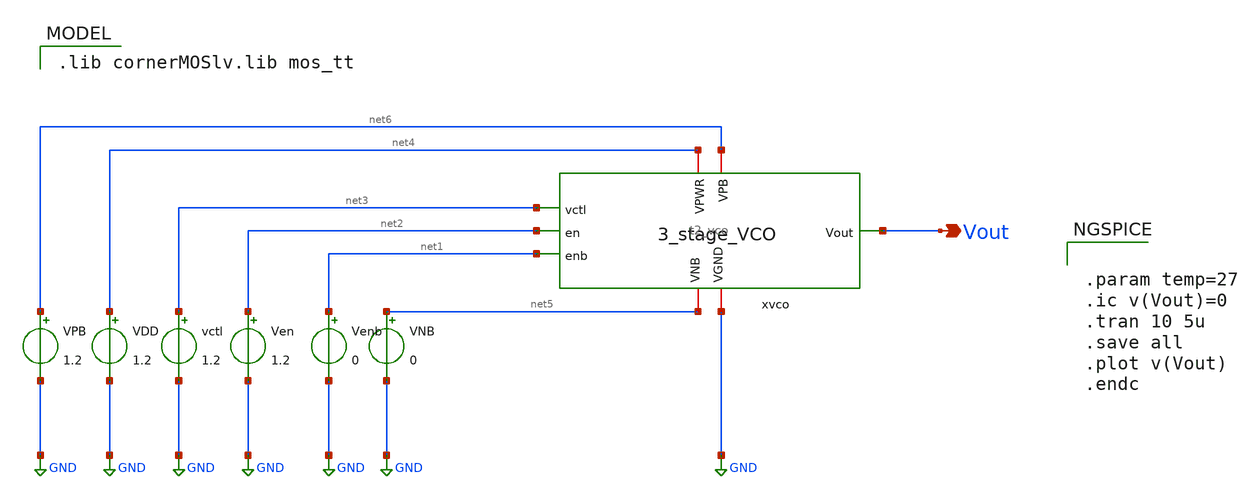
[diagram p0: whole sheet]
** sch_path: Team 2 Design/design_data/xschem/t2_vco_tb.sch
**.subckt t2_vco_tb Vout
*.opin Vout
VDD net4 GND 1.2
vctl net3 GND 1.2
Ven net2 GND 1.2
Venb net1 GND 0
VNB net5 GND 0
VPB net6 GND 1.2
x1 net4 net6 GND net5 Vout net3 net2 net1 t2_vco
**** begin user architecture code
 .lib cornerMOSlv.lib mos_tt



.param temp=27
.ic v(Vout)=0
.tran 10 5u
.save all
.plot v(Vout)
.endc


**** end user architecture code
**.ends
.GLOBAL GND
.end
